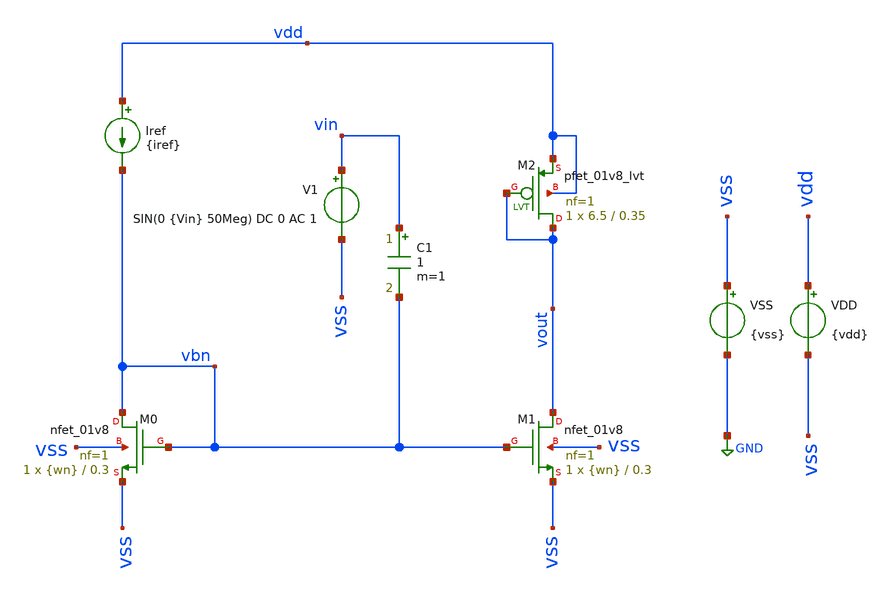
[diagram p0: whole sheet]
** sch_path: tp2/tp2_5_b.sch
**.subckt tp2_5_b
Iref vdd vbn {iref}
VSS vss GND {vss}
VDD vdd vss {vdd}
V1 vin vss SIN(0 {Vin} 50Meg) DC 0 AC 1
XM1 vout vbn vss vss sky130_fd_pr__nfet_01v8 L=0.3 W={wn} nf=1 ad='int((nf+1)/2) * W/nf * 0.29' as='int((nf+2)/2) * W/nf * 0.29'
+ pd='2*int((nf+1)/2) * (W/nf + 0.29)' ps='2*int((nf+2)/2) * (W/nf + 0.29)' nrd='0.29 / W' nrs='0.29 / W'
+ sa=0 sb=0 sd=0 mult=1 m=1
XM0 vbn vbn vss vss sky130_fd_pr__nfet_01v8 L=0.3 W={wn} nf=1 ad='int((nf+1)/2) * W/nf * 0.29' as='int((nf+2)/2) * W/nf * 0.29'
+ pd='2*int((nf+1)/2) * (W/nf + 0.29)' ps='2*int((nf+2)/2) * (W/nf + 0.29)' nrd='0.29 / W' nrs='0.29 / W'
+ sa=0 sb=0 sd=0 mult=1 m=1
C1 vin vbn 1 m=1
XM2 vout vout vdd vdd sky130_fd_pr__pfet_01v8_lvt L=0.35 W=6.5 nf=1 ad='int((nf+1)/2) * W/nf * 0.29'
+ as='int((nf+2)/2) * W/nf * 0.29' pd='2*int((nf+1)/2) * (W/nf + 0.29)' ps='2*int((nf+2)/2) * (W/nf + 0.29)'
+ nrd='0.29 / W' nrs='0.29 / W' sa=0 sb=0 sd=0 mult=1 m=1
**** begin user architecture code



* Parameters
.param vdd = 1.8
.param vss = 0.0
.param iref = 200u
.param wn = 6.46
.param R = 4.5k
.param Vin = 40m

.options TEMP = 65.0

* Models
*.lib ~/skywater/skywater-pdk/libraries/sky130_fd_pr_ngspice/latest/models/corners/sky130.lib TT
.lib /foss/pdks/sky130A/libs.tech/ngspice/sky130.lib.spice tt
* Data to save
.save all  @M.XM0.msky130_fd_pr__nfet_01v8[id]  @M.XM0.msky130_fd_pr__nfet_01v8[vds]  @M.XM0.msky130_fd_pr__nfet_01v8[vgs]  @M.XM0.msky130_fd_pr__nfet_01v8[vdsat]  @M.XM0.msky130_fd_pr__nfet_01v8[vth]  @M.XM0.msky130_fd_pr__nfet_01v8[gm]  @M.XM1.msky130_fd_pr__nfet_01v8[id]  @M.XM1.msky130_fd_pr__nfet_01v8[vds]  @M.XM1.msky130_fd_pr__nfet_01v8[vgs]  @M.XM1.msky130_fd_pr__nfet_01v8[vdsat]  @M.XM1.msky130_fd_pr__nfet_01v8[vth]  @M.XM1.msky130_fd_pr__nfet_01v8[gm]  @M.XM1.msky130_fd_pr__nfet_01v8[gds]  @M.XM2.msky130_fd_pr__pfet_01v8_lvt[id]  @M.XM2.msky130_fd_pr__pfet_01v8_lvt[vds]  @M.XM2.msky130_fd_pr__pfet_01v8_lvt[vgs]  @M.XM2.msky130_fd_pr__pfet_01v8_lvt[vdsat]  @M.XM2.msky130_fd_pr__pfet_01v8_lvt[vth]  @M.XM2.msky130_fd_pr__pfet_01v8_lvt[gm]  @M.XM2.msky130_fd_pr__pfet_01v8_lvt[gds]



* Simulation
.control
  ac dec 100 10k 100G
  setplot ac1
  plot vdb(vout) {vp(vout)*180/PI}
  meas ac DCG find v(vout) at=50meg
  write tp2_5_ac.raw

  reset
  tran 0.01n 100n
  plot v(vbn) v(vout) v(vin)
  write tp2_5_tran.raw

  reset
  op
  save all
  print all
  unset filetype
  write tp2_5_b.raw
.endc

.end


**** end user architecture code
**.ends
.GLOBAL GND
.end
